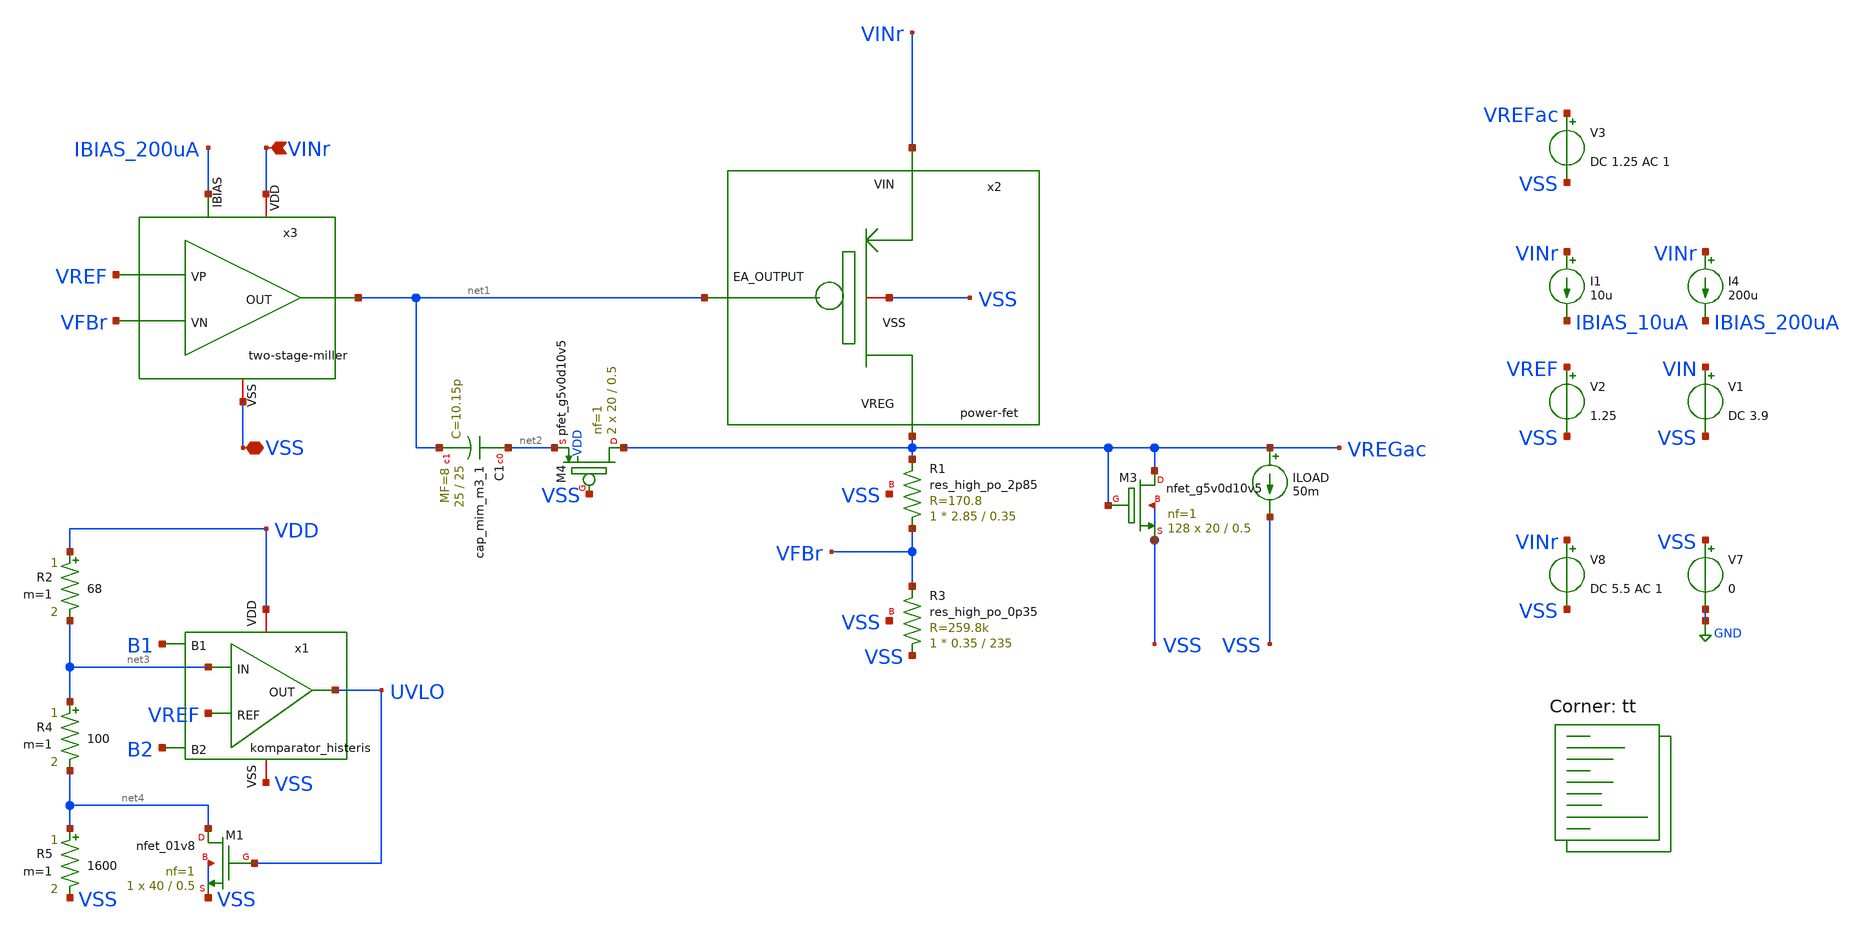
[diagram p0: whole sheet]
** sch_path: bandgap/testbench/ldo-psrr.sch
**.subckt ldo-psrr VINr VSS
*.ipin VINr
*.iopin VSS
V2 VREF VSS 1.25
V7 VSS GND 0
V8 VINr VSS DC 5.5 AC 1
I4 VINr IBIAS_200uA 200u
I1 VINr IBIAS_10uA 10u
V1 VIN VSS DC 3.9
V3 VREFac VSS DC 1.25 AC 1
x2 VINr VSS net1 VREGac power-fet
XR3 VSS VFBr VSS sky130_fd_pr__res_high_po_0p35 L=235 mult=1 m=1
XR1 VFBr VREGac VSS sky130_fd_pr__res_high_po_2p85 L=0.35 mult=1 m=1
x3 VINr net1 VREF VFBr IBIAS_200uA VSS two-stage-miller
ILOAD VREGac VSS 50m
XM3 VREGac VREGac VSS VSS sky130_fd_pr__nfet_g5v0d10v5 L=0.5 W=20 nf=1 ad='int((nf+1)/2) * W/nf * 0.29'
+ as='int((nf+2)/2) * W/nf * 0.29' pd='2*int((nf+1)/2) * (W/nf + 0.29)' ps='2*int((nf+2)/2) * (W/nf + 0.29)'
+ nrd='0.29 / W' nrs='0.29 / W' sa=0 sb=0 sd=0 mult=128 m=128
XC1 net2 net1 sky130_fd_pr__cap_mim_m3_1 W=25 L=25 MF=8 m=8
XM4 VREGac VSS net2 VDD sky130_fd_pr__pfet_g5v0d10v5 L=0.5 W=20 nf=1 ad='int((nf+1)/2) * W/nf * 0.29'
+ as='int((nf+2)/2) * W/nf * 0.29' pd='2*int((nf+1)/2) * (W/nf + 0.29)' ps='2*int((nf+2)/2) * (W/nf + 0.29)'
+ nrd='0.29 / W' nrs='0.29 / W' sa=0 sb=0 sd=0 mult=2 m=2
R2 VDD net3 68 m=1
R4 net3 net4 100 m=1
R5 net4 VSS 1600 m=1
XM1 net4 UVLO VSS VSS sky130_fd_pr__nfet_01v8 L=0.5 W=40 nf=1 ad='int((1 + 1)/2) * 40 / 1 * 0.29' as='int((1 + 2)/2) * 40 / 1 * 0.29'
+ pd='2*int((1 + 1)/2) * (40 / 1 + 0.29)' ps='2*int((1 + 2)/2) * (40 / 1 + 0.29)' nrd='0.29 / 40 ' nrs='0.29 / 40 '
+ sa=0 sb=0 sd=0 mult=1 m=1
x1 VDD VREF net3 UVLO B1 B2 VSS komparator_histeris
**** begin user architecture code


.temp 27
.control
    * Lakukan simulasi AC
    AC DEC 100 1 100G

    * 1. Menghitung PSRR yang Benar
    * PSRR = Gain dari Supply ke Output (VREG).
    * Biasanya kita ingin melihat penolakan (rejection), jadi kita hitung 1/Gain.
    * Jika input AC supply (Vripple) = 1V, maka PSRR_db = -db(v(VREGac))
    let psrr_plot = -db(v(VREGac))

    * 2. Menghitung Loop Gain & Phase Margin
    * Pastikan v(PROBE) adalah node setelah injeksi AC (Tian Method / Middlebrook)
    let loop_gain_complex = v(PROBE)
    let lg_db = db(loop_gain_complex)
    * ph(x) di ngspice hasilnya dalam radian, kita ubah ke derajat
    let lg_ph = ph(loop_gain_complex) * 180 / PI

    * Phase Margin biasanya diukur dari jarak fase ke -180 derajat
    let phase_margin_plot = lg_ph + 180

    * 3. Pengukuran Otomatis (MEAS)
    * Cari Unity Gain Frequency (UGF)
    meas ac f_unity when lg_db=0

    * Cari Phase Margin pada frekuensi f_unity tersebut
    * Gunakan 'at' dengan variabel yang sudah didapat dari f_unity
    meas ac PM_value find phase_margin_plot at=f_unity

    * 4. Menghitung PSRR pada Berbagai Band
    * Ingat: Gunakan let psrr_plot yang sudah didefinisikan agar tidak redundan
    meas ac psrr_dc find psrr_plot at=1
    meas ac psrr_100k find psrr_plot at=100k
    meas ac psrr_1M find psrr_plot at=1meg

    * 5. Cetak Hasil ke Terminal
    echo ======================================
    echo Unity Gain Frequency: $&f_unity Hz
    echo Phase Margin: $&PM_value degrees
    echo PSRR at DC: $&psrr_dc dB
    echo PSRR at 100kHz: $&psrr_100k dB
    echo PSRR at 1MHz: $&psrr_1M dB
    echo ======================================

    * 6. Plotting
    plot lg_db phase_margin_plot ylimit -50 100 title 'Loop Gain and Phase'
    plot psrr_plot title 'Power Supply Rejection Ratio (dB)'

.endc


.lib $::SKYWATER_MODELS/sky130.lib.spice tt
**** end user architecture code
**.ends
.GLOBAL GND
.end
